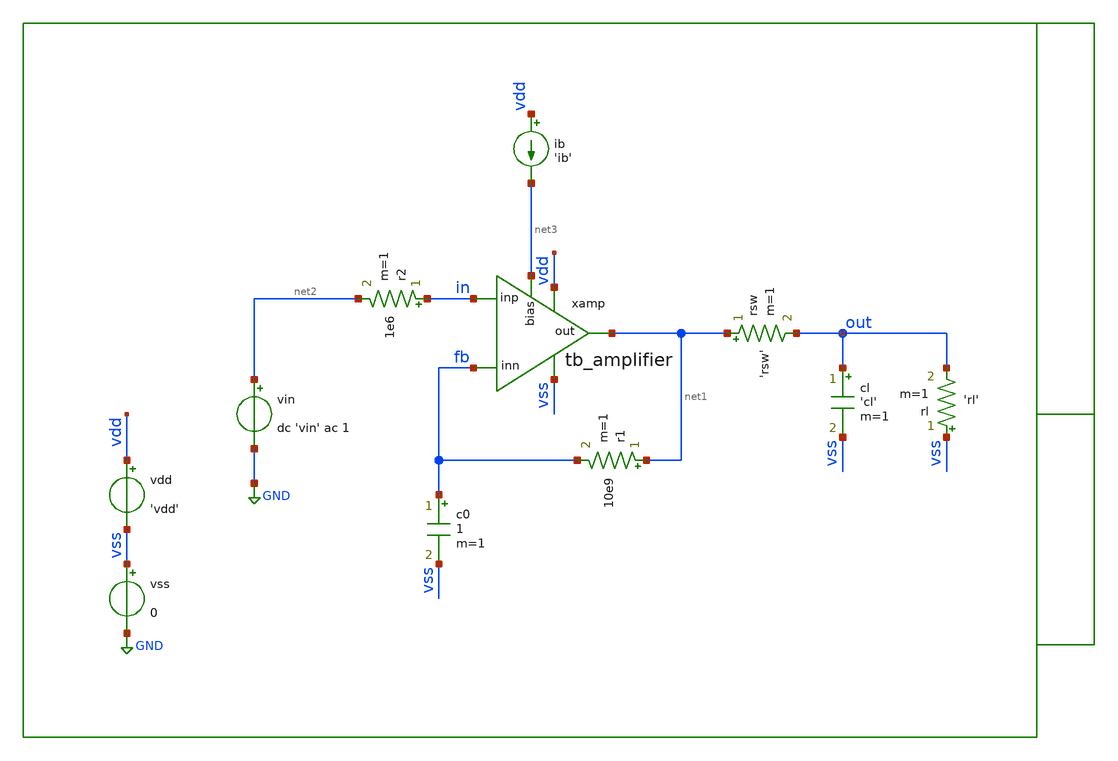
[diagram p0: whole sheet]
** sch_path: xschem/tb/testbuffer/tb_amplifier/ac_tb_amplifier_cin.sch
**.subckt ac_tb_amplifier_cin
vdd vdd vss 'vdd'
vss vss GND 0
vin net2 GND dc 'vin' ac 1
c0 fb vss 1 m=1
r1 net1 fb 10e9 m=1
cl out vss 'cl' m=1
ib vdd net3 'ib'
rl vss out 'rl' m=1
xamp vdd net1 in fb vss net3 tb_amplifier
rsw net1 out 'rsw' m=1
r2 in net2 1e6 m=1
**** begin user architecture code

* Control

.param vdd=3.3
.param vcm='vdd/2'
.param vin='vcm'
.param ib=5u
.param cl=10p
.param rl=1e6
.param rsw=1

.control

ac dec 100 1 1e9

meas ac fbw when vdb(in)=-3
let cin = 1/(2*PI*1e6*fbw)

print cin
gnuplot p1 vdb(in)

.endc


 * Model Corners

.include $::CORNERS/ngspice/tt.spice
*.include $::CORNERS/ngspice/ff.spice
*.include $::CORNERS/ngspice/ss.spice
*.include $::CORNERS/ngspice/sf.spice
*.include $::CORNERS/ngspice/fs.spice

**** end user architecture code
**.ends

* expanding   symbol:  sch/testbuffer/tb_amplifier/tb_amplifier.sym # of pins=6
** sym_path: xschem/sch/testbuffer/tb_amplifier/tb_amplifier.sym
** sch_path: xschem/sch/testbuffer/tb_amplifier/tb_amplifier.sch
.subckt tb_amplifier vdd out inp inn vss bias
*.ipin inn
*.ipin inp
*.opin out
*.iopin bias
*.iopin vdd
*.iopin vss
XM3 mirr mirr vdd vdd pfet_06v0 L=4u W=16u nf=2 ad='int((nf+1)/2) * W/nf * 0.18u' as='int((nf+2)/2) * W/nf * 0.18u'
+ pd='2*int((nf+1)/2) * (W/nf + 0.18u)' ps='2*int((nf+2)/2) * (W/nf + 0.18u)' nrd='0.18u / W' nrs='0.18u / W'
+ sa=0 sb=0 sd=0 m=2 par=2
XM4 comp mirr vdd vdd pfet_06v0 L=4u W=16u nf=2 ad='int((nf+1)/2) * W/nf * 0.18u' as='int((nf+2)/2) * W/nf * 0.18u'
+ pd='2*int((nf+1)/2) * (W/nf + 0.18u)' ps='2*int((nf+2)/2) * (W/nf + 0.18u)' nrd='0.18u / W' nrs='0.18u / W'
+ sa=0 sb=0 sd=0 m=2 par=2
XM2 comp inp vcm vss nfet_06v0 L=2u W=16u nf=2 ad='int((nf+1)/2) * W/nf * 0.18u' as='int((nf+2)/2) * W/nf * 0.18u'
+ pd='2*int((nf+1)/2) * (W/nf + 0.18u)' ps='2*int((nf+2)/2) * (W/nf + 0.18u)' nrd='0.18u / W' nrs='0.18u / W'
+ sa=0 sb=0 sd=0 m=2 par=2
XM1 mirr inn vcm vss nfet_06v0 L=2u W=16u nf=2 ad='int((nf+1)/2) * W/nf * 0.18u' as='int((nf+2)/2) * W/nf * 0.18u'
+ pd='2*int((nf+1)/2) * (W/nf + 0.18u)' ps='2*int((nf+2)/2) * (W/nf + 0.18u)' nrd='0.18u / W' nrs='0.18u / W'
+ sa=0 sb=0 sd=0 m=2 par=2
XM5 vcm bias vss vss nfet_06v0 L=1u W=16u nf=2 ad='int((nf+1)/2) * W/nf * 0.18u' as='int((nf+2)/2) * W/nf * 0.18u'
+ pd='2*int((nf+1)/2) * (W/nf + 0.18u)' ps='2*int((nf+2)/2) * (W/nf + 0.18u)' nrd='0.18u / W' nrs='0.18u / W'
+ sa=0 sb=0 sd=0 m=2 par=2
XM6 out bias vss vss nfet_06v0 L=1u W=16u nf=2 ad='int((nf+1)/2) * W/nf * 0.18u' as='int((nf+2)/2) * W/nf * 0.18u'
+ pd='2*int((nf+1)/2) * (W/nf + 0.18u)' ps='2*int((nf+2)/2) * (W/nf + 0.18u)' nrd='0.18u / W' nrs='0.18u / W'
+ sa=0 sb=0 sd=0 m=12 par=12
XM7 out comp vdd vdd pfet_06v0 L=1u W=96u nf=12 ad='int((nf+1)/2) * W/nf * 0.18u' as='int((nf+2)/2) * W/nf * 0.18u'
+ pd='2*int((nf+1)/2) * (W/nf + 0.18u)' ps='2*int((nf+2)/2) * (W/nf + 0.18u)' nrd='0.18u / W' nrs='0.18u / W'
+ sa=0 sb=0 sd=0 m=1 par=1
XMB1 bias bias vss vss nfet_06v0 L=1u W=16u nf=2 ad='int((nf+1)/2) * W/nf * 0.18u' as='int((nf+2)/2) * W/nf * 0.18u'
+ pd='2*int((nf+1)/2) * (W/nf + 0.18u)' ps='2*int((nf+2)/2) * (W/nf + 0.18u)' nrd='0.18u / W' nrs='0.18u / W'
+ sa=0 sb=0 sd=0 m=2 par=2
XMB2 vbm bias vss vss nfet_06v0 L=1u W=16u nf=2 ad='int((nf+1)/2) * W/nf * 0.18u' as='int((nf+2)/2) * W/nf * 0.18u'
+ pd='2*int((nf+1)/2) * (W/nf + 0.18u)' ps='2*int((nf+2)/2) * (W/nf + 0.18u)' nrd='0.18u / W' nrs='0.18u / W'
+ sa=0 sb=0 sd=0 m=2 par=2
XMB3 vbm vbm vbt vdd pfet_06v0 L=1u W=16u nf=2 ad='int((nf+1)/2) * W/nf * 0.18u' as='int((nf+2)/2) * W/nf * 0.18u'
+ pd='2*int((nf+1)/2) * (W/nf + 0.18u)' ps='2*int((nf+2)/2) * (W/nf + 0.18u)' nrd='0.18u / W' nrs='0.18u / W'
+ sa=0 sb=0 sd=0 m=1 par=1
XMB4 vbt vbt vdd vdd pfet_06v0 L=1u W=16u nf=2 ad='int((nf+1)/2) * W/nf * 0.18u' as='int((nf+2)/2) * W/nf * 0.18u'
+ pd='2*int((nf+1)/2) * (W/nf + 0.18u)' ps='2*int((nf+2)/2) * (W/nf + 0.18u)' nrd='0.18u / W' nrs='0.18u / W'
+ sa=0 sb=0 sd=0 m=1 par=1
XRCC gc comp vdd ppolyf_u_1k_6p0 r_width=2e-6 r_length=38e-6 s=1 m=1
XMDUM1 vss vss vss vss nfet_06v0 L=2u W=16u nf=2 ad='int((nf+1)/2) * W/nf * 0.18u' as='int((nf+2)/2) * W/nf * 0.18u'
+ pd='2*int((nf+1)/2) * (W/nf + 0.18u)' ps='2*int((nf+2)/2) * (W/nf + 0.18u)' nrd='0.18u / W' nrs='0.18u / W'
+ sa=0 sb=0 sd=0 m=2 par=2
XMDUM2 vdd vdd vdd vdd pfet_06v0 L=4u W=16u nf=2 ad='int((nf+1)/2) * W/nf * 0.18u' as='int((nf+2)/2) * W/nf * 0.18u'
+ pd='2*int((nf+1)/2) * (W/nf + 0.18u)' ps='2*int((nf+2)/2) * (W/nf + 0.18u)' nrd='0.18u / W' nrs='0.18u / W'
+ sa=0 sb=0 sd=0 m=4 par=4
XC1 out gc cap_mim_2f0_m4m5_noshield c_width=30e-6 c_length=30e-6 m=1
.ends

.GLOBAL GND
.end
